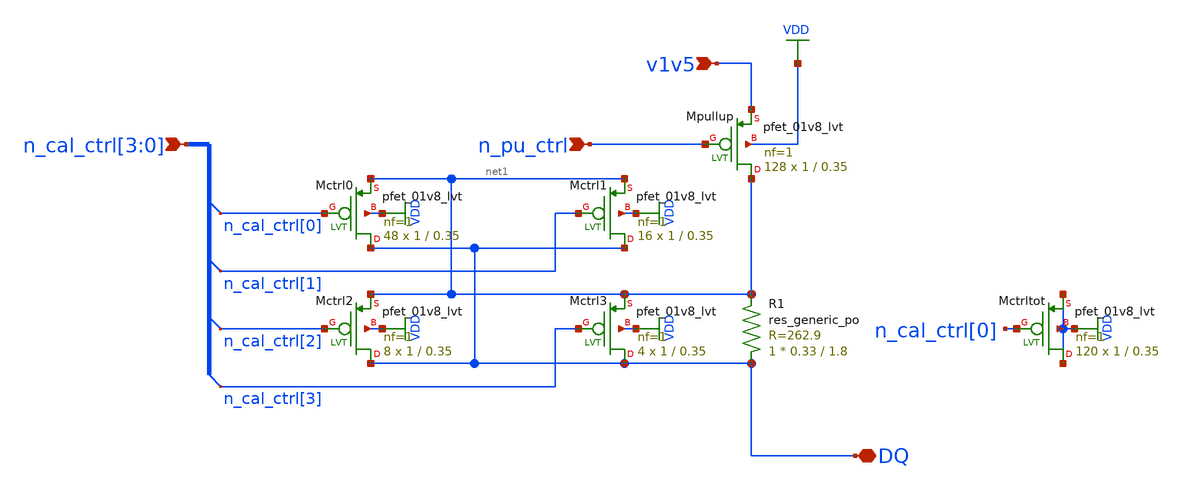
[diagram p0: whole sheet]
** sch_path: p-leg.sch
* Copyright 2021 Stefan Frederik Schippers
* Licensed under the Apache License, Version 2.0 (the "License");
* you may not use this file except in compliance with the License.
* You may obtain a copy of the License at
* https://www.apache.org/licenses/LICENSE-2.0
* Unless required by applicable law or agreed to in writing, software
* distributed under the License is distributed on an "AS IS" BASIS,
* WITHOUT WARRANTIES OR CONDITIONS OF ANY KIND, either express or implied.
* See the License for the specific language governing permissions and
* limitations under the License.
**.subckt p-leg n_cal_ctrl[3],n_cal_ctrl[2],n_cal_ctrl[1],n_cal_ctrl[0] n_pu_ctrl DQ v1v5
*.ipin n_cal_ctrl[3],n_cal_ctrl[2],n_cal_ctrl[1],n_cal_ctrl[0]
*.ipin n_pu_ctrl
*.iopin DQ
*.ipin v1v5
XR1 DQ net1 sky130_fd_pr__res_generic_po W=0.33 L=1.8 m=1
XMpullup net1 n_pu_ctrl v1v5 VDD sky130_fd_pr__pfet_01v8_lvt L=0.35 W=1 nf=1 ad='int((nf+1)/2) * W/nf * 0.29'
+ as='int((nf+2)/2) * W/nf * 0.29' pd='2*int((nf+1)/2) * (W/nf + 0.29)' ps='2*int((nf+2)/2) * (W/nf + 0.29)'
+ nrd='0.29 / W' nrs='0.29 / W' sa=0 sb=0 sd=0 mult=128 m=128
XMctrltot VDD n_cal_ctrl[0] VDD VDD sky130_fd_pr__pfet_01v8_lvt L=0.35 W=1 nf=1 ad='int((nf+1)/2) * W/nf * 0.29'
+ as='int((nf+2)/2) * W/nf * 0.29' pd='2*int((nf+1)/2) * (W/nf + 0.29)' ps='2*int((nf+2)/2) * (W/nf + 0.29)'
+ nrd='0.29 / W' nrs='0.29 / W' sa=0 sb=0 sd=0 mult=120 m=120
XMctrl0 DQ n_cal_ctrl[0] net1 VDD sky130_fd_pr__pfet_01v8_lvt L=0.35 W=1 nf=1 ad='int((nf+1)/2) * W/nf * 0.29'
+ as='int((nf+2)/2) * W/nf * 0.29' pd='2*int((nf+1)/2) * (W/nf + 0.29)' ps='2*int((nf+2)/2) * (W/nf + 0.29)'
+ nrd='0.29 / W' nrs='0.29 / W' sa=0 sb=0 sd=0 mult=48 m=48
XMctrl1 DQ n_cal_ctrl[1] net1 VDD sky130_fd_pr__pfet_01v8_lvt L=0.35 W=1 nf=1 ad='int((nf+1)/2) * W/nf * 0.29'
+ as='int((nf+2)/2) * W/nf * 0.29' pd='2*int((nf+1)/2) * (W/nf + 0.29)' ps='2*int((nf+2)/2) * (W/nf + 0.29)'
+ nrd='0.29 / W' nrs='0.29 / W' sa=0 sb=0 sd=0 mult=16 m=16
XMctrl2 DQ n_cal_ctrl[2] net1 VDD sky130_fd_pr__pfet_01v8_lvt L=0.35 W=1 nf=1 ad='int((nf+1)/2) * W/nf * 0.29'
+ as='int((nf+2)/2) * W/nf * 0.29' pd='2*int((nf+1)/2) * (W/nf + 0.29)' ps='2*int((nf+2)/2) * (W/nf + 0.29)'
+ nrd='0.29 / W' nrs='0.29 / W' sa=0 sb=0 sd=0 mult=8 m=8
XMctrl3 DQ n_cal_ctrl[3] net1 VDD sky130_fd_pr__pfet_01v8_lvt L=0.35 W=1 nf=1 ad='int((nf+1)/2) * W/nf * 0.29'
+ as='int((nf+2)/2) * W/nf * 0.29' pd='2*int((nf+1)/2) * (W/nf + 0.29)' ps='2*int((nf+2)/2) * (W/nf + 0.29)'
+ nrd='0.29 / W' nrs='0.29 / W' sa=0 sb=0 sd=0 mult=4 m=4
**.ends
.GLOBAL VDD
.end
